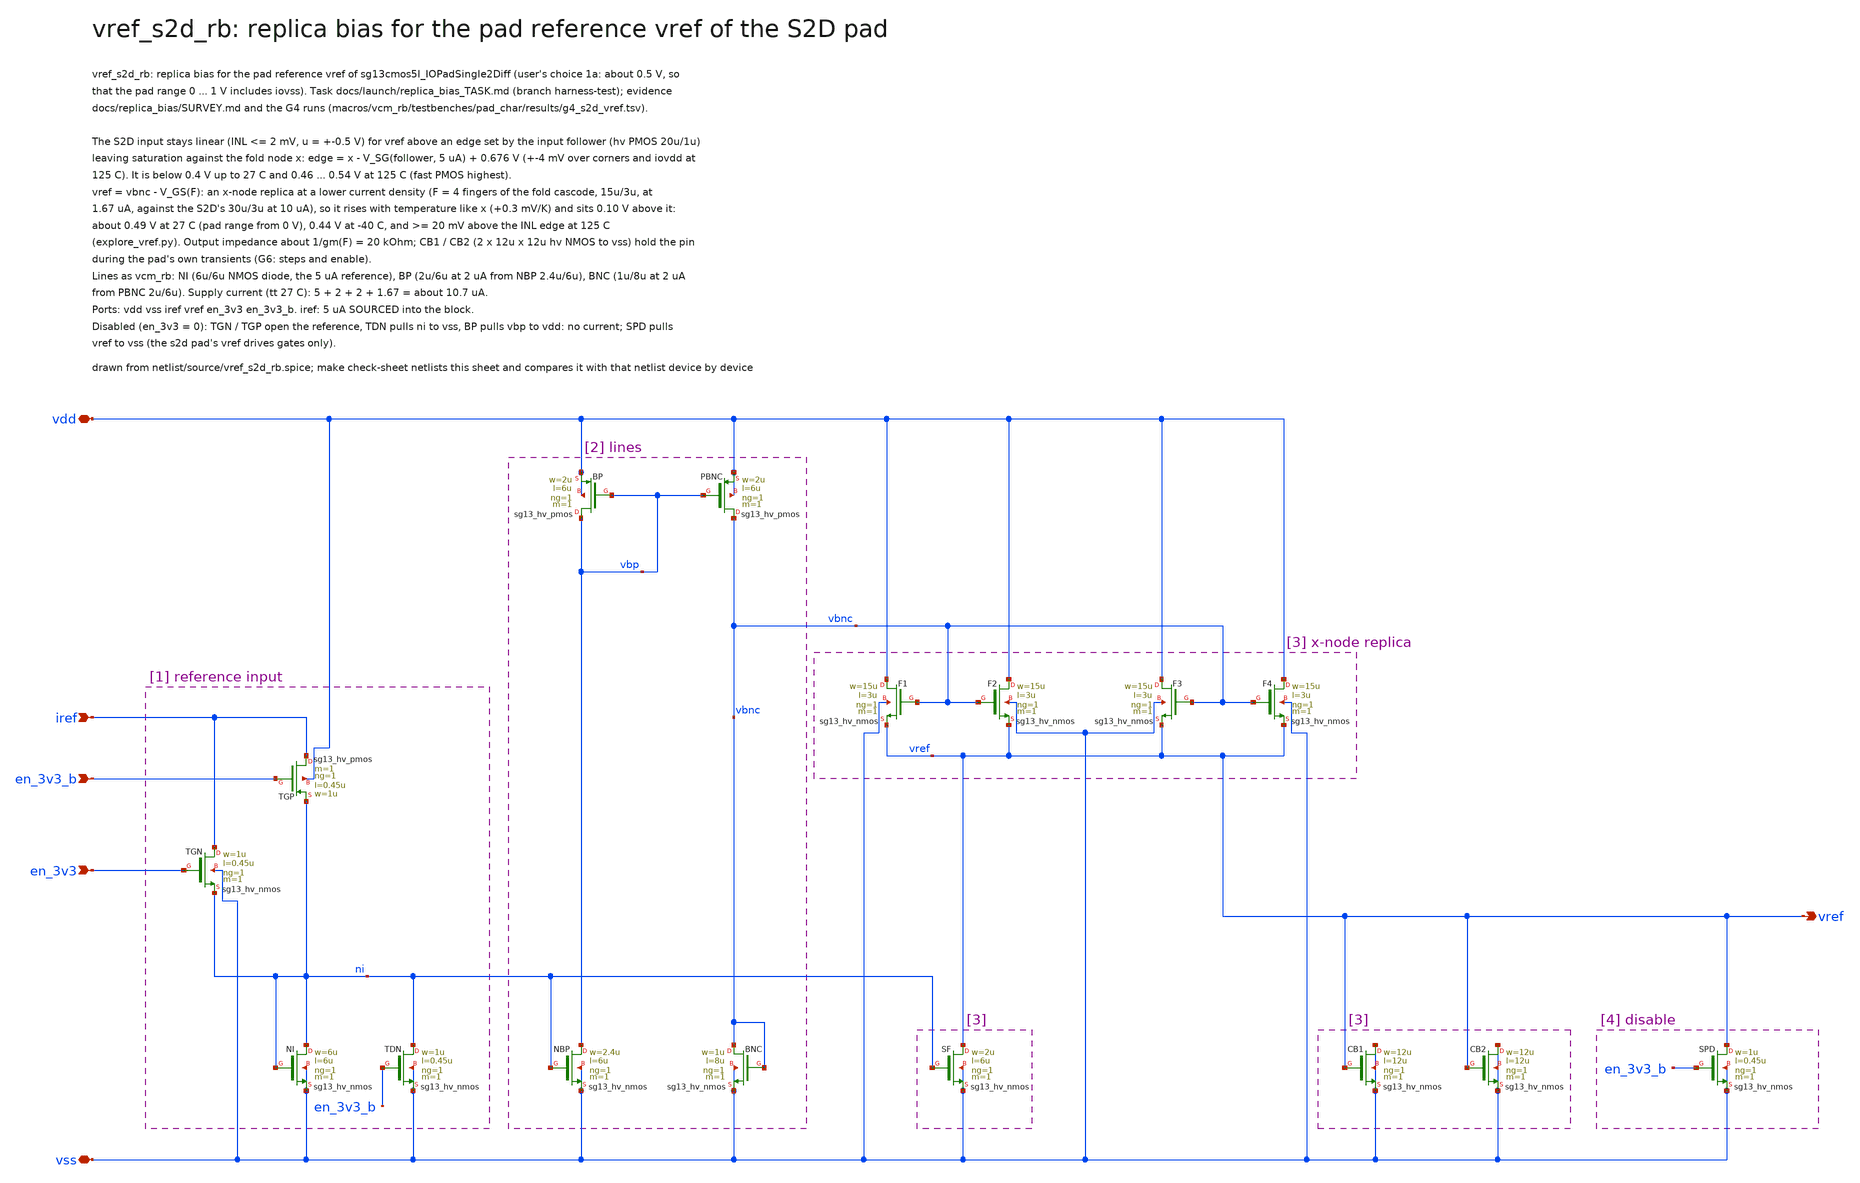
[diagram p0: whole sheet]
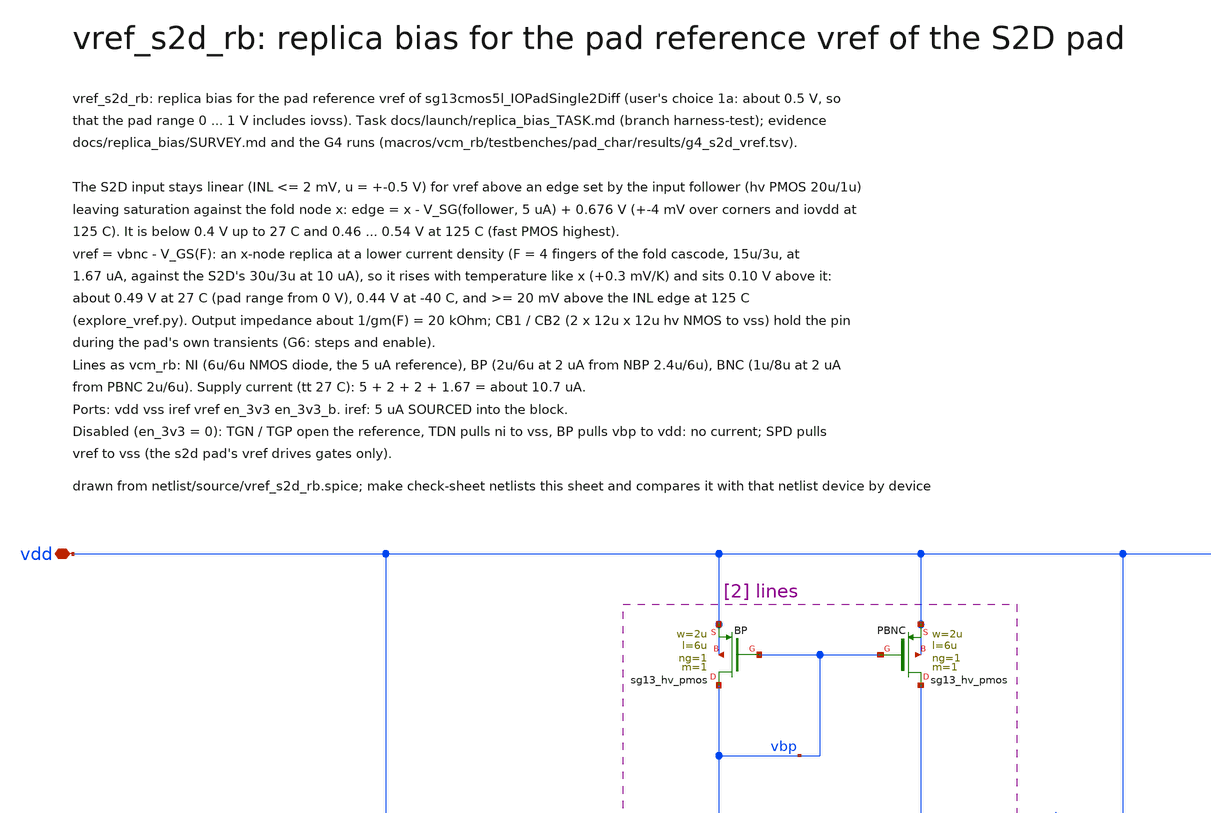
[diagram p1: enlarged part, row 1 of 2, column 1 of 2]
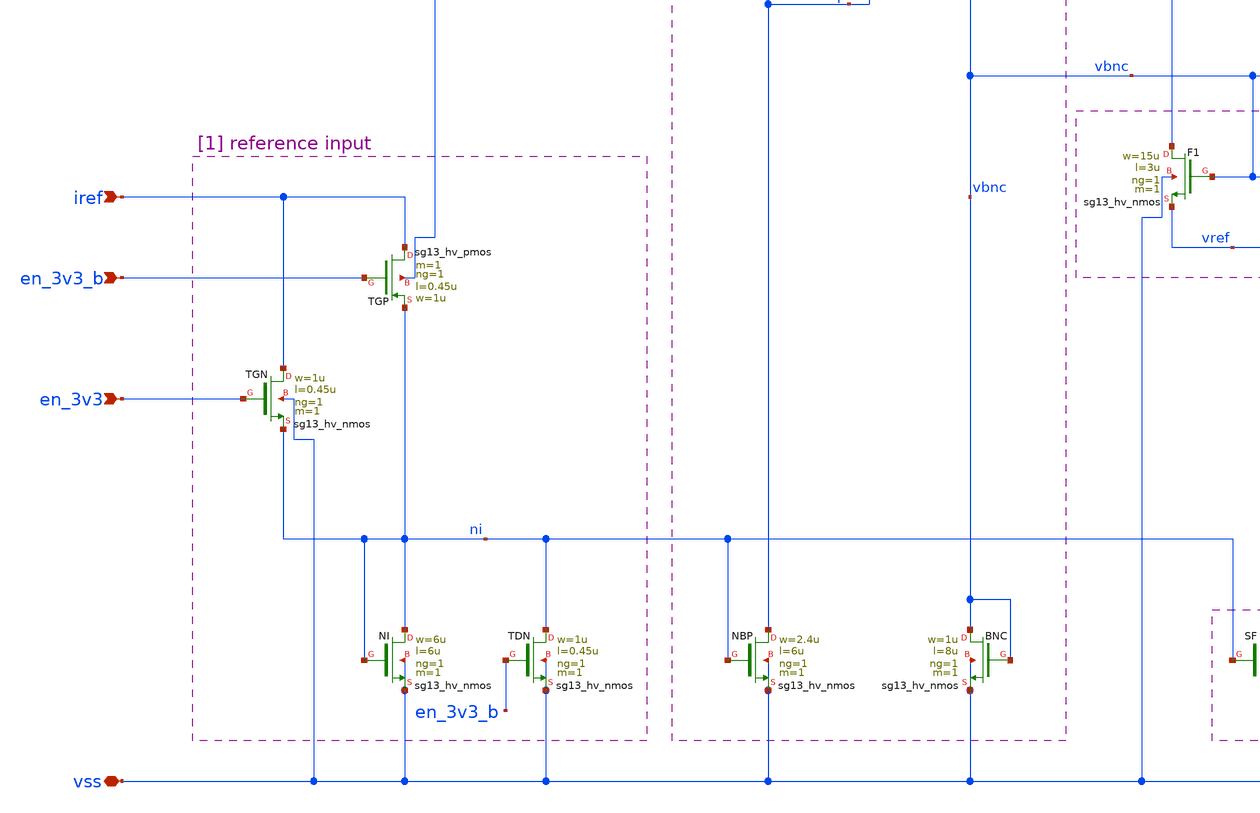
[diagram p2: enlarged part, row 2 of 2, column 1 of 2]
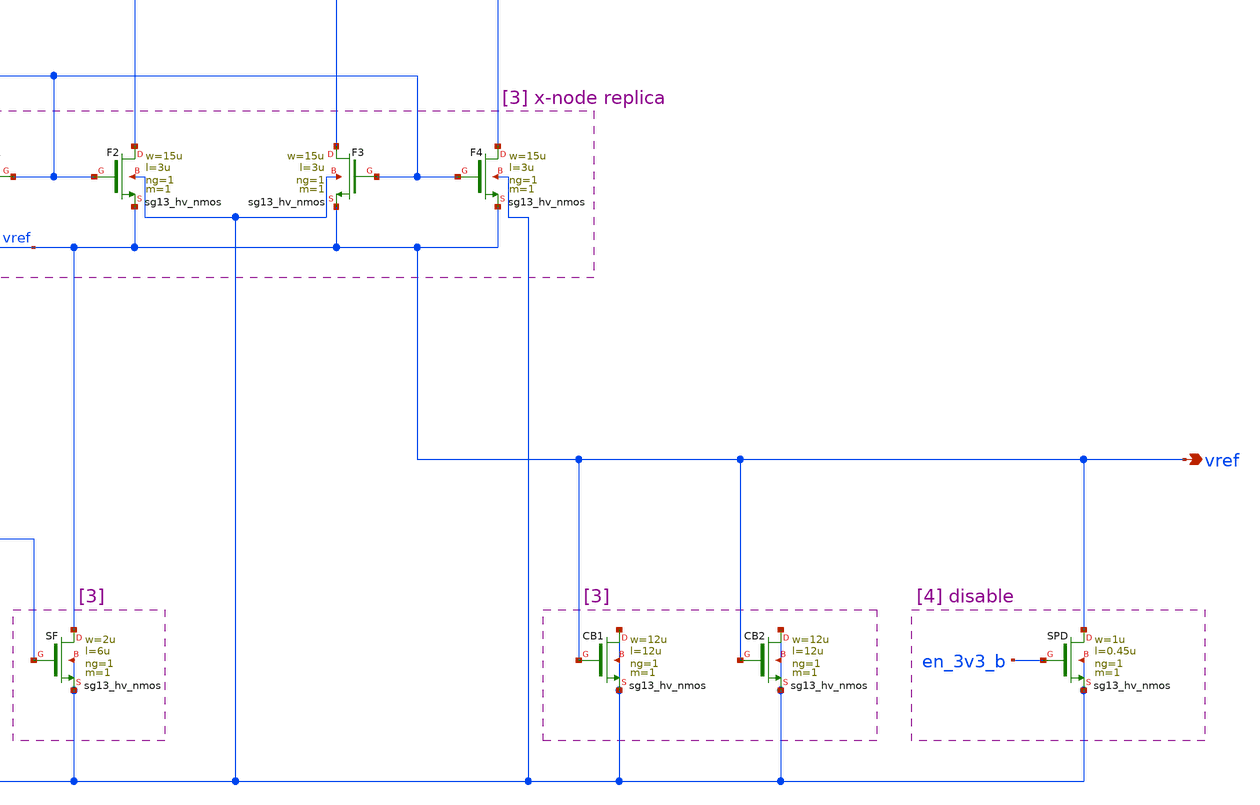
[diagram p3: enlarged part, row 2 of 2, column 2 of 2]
** sch_path: macros/vref_s2d_rb/schematic/xschem/vref_s2d_rb.sch
**.subckt vref_s2d_rb vdd vss iref vref en_3v3 en_3v3_b
*.iopin vdd
*.iopin vss
*.ipin iref
*.opin vref
*.ipin en_3v3
*.ipin en_3v3_b
XTGN iref en_3v3 ni vss sg13_hv_nmos w=1u l=0.45u ng=1 m=1 mm_ok=1
XTGP iref en_3v3_b ni vdd sg13_hv_pmos w=1u l=0.45u ng=1 m=1 mm_ok=1
XTDN ni en_3v3_b vss vss sg13_hv_nmos w=1u l=0.45u ng=1 m=1 mm_ok=1
XNI ni ni vss vss sg13_hv_nmos w=6u l=6u ng=1 m=1 mm_ok=1
XNBP vbp ni vss vss sg13_hv_nmos w=2.4u l=6u ng=1 m=1 mm_ok=1
XBP vbp vbp vdd vdd sg13_hv_pmos w=2u l=6u ng=1 m=1 mm_ok=1
XPBNC vbnc vbp vdd vdd sg13_hv_pmos w=2u l=6u ng=1 m=1 mm_ok=1
XBNC vbnc vbnc vss vss sg13_hv_nmos w=1u l=8u ng=1 m=1 mm_ok=1
XF1 vdd vbnc vref vss sg13_hv_nmos w=15u l=3u ng=1 m=1 mm_ok=1
XF2 vdd vbnc vref vss sg13_hv_nmos w=15u l=3u ng=1 m=1 mm_ok=1
XF3 vdd vbnc vref vss sg13_hv_nmos w=15u l=3u ng=1 m=1 mm_ok=1
XF4 vdd vbnc vref vss sg13_hv_nmos w=15u l=3u ng=1 m=1 mm_ok=1
XSF vref ni vss vss sg13_hv_nmos w=2u l=6u ng=1 m=1 mm_ok=1
XCB1 vss vref vss vss sg13_hv_nmos w=12u l=12u ng=1 m=1 mm_ok=1
XCB2 vss vref vss vss sg13_hv_nmos w=12u l=12u ng=1 m=1 mm_ok=1
XSPD vref en_3v3_b vss vss sg13_hv_nmos w=1u l=0.45u ng=1 m=1 mm_ok=1
**.ends
.end
